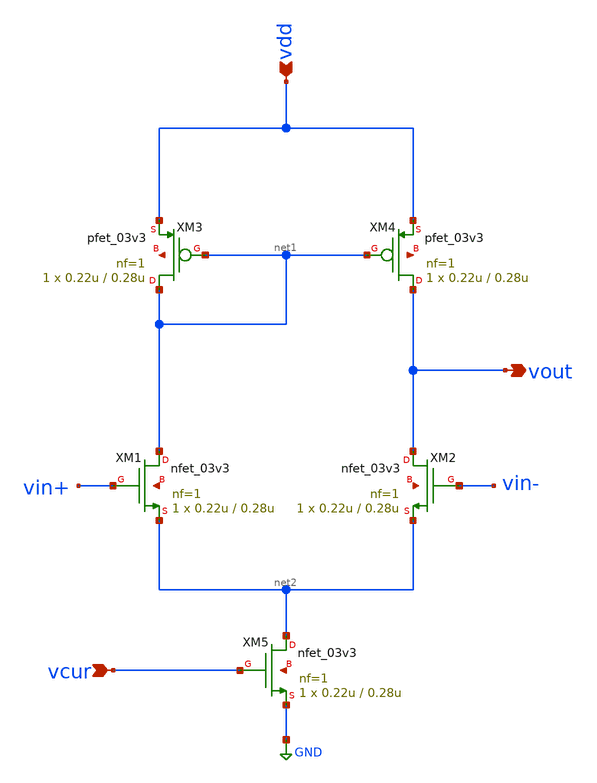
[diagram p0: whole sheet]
** sch_path: designs/5tOTA.sch
**.subckt 5tOTA vdd vout vcur
*.ipin vdd
*.opin vout
*.ipin vcur
XM1 net1 vin+ net2 net3 nfet_03v3 L=0.28u W=0.22u nf=1 ad='int((nf+1)/2) * W/nf * 0.18u' as='int((nf+2)/2) * W/nf * 0.18u'
+ pd='2*int((nf+1)/2) * (W/nf + 0.18u)' ps='2*int((nf+2)/2) * (W/nf + 0.18u)' nrd='0.18u / W' nrs='0.18u / W'
+ sa=0 sb=0 sd=0 m=1
XM2 vout vin- net2 net4 nfet_03v3 L=0.28u W=0.22u nf=1 ad='int((nf+1)/2) * W/nf * 0.18u' as='int((nf+2)/2) * W/nf * 0.18u'
+ pd='2*int((nf+1)/2) * (W/nf + 0.18u)' ps='2*int((nf+2)/2) * (W/nf + 0.18u)' nrd='0.18u / W' nrs='0.18u / W'
+ sa=0 sb=0 sd=0 m=1
XM3 net1 net1 vdd net5 pfet_03v3 L=0.28u W=0.22u nf=1 ad='int((nf+1)/2) * W/nf * 0.18u' as='int((nf+2)/2) * W/nf * 0.18u'
+ pd='2*int((nf+1)/2) * (W/nf + 0.18u)' ps='2*int((nf+2)/2) * (W/nf + 0.18u)' nrd='0.18u / W' nrs='0.18u / W'
+ sa=0 sb=0 sd=0 m=1
XM4 vout net1 vdd net6 pfet_03v3 L=0.28u W=0.22u nf=1 ad='int((nf+1)/2) * W/nf * 0.18u' as='int((nf+2)/2) * W/nf * 0.18u'
+ pd='2*int((nf+1)/2) * (W/nf + 0.18u)' ps='2*int((nf+2)/2) * (W/nf + 0.18u)' nrd='0.18u / W' nrs='0.18u / W'
+ sa=0 sb=0 sd=0 m=1
XM5 net2 vcur GND net7 nfet_03v3 L=0.28u W=0.22u nf=1 ad='int((nf+1)/2) * W/nf * 0.18u' as='int((nf+2)/2) * W/nf * 0.18u'
+ pd='2*int((nf+1)/2) * (W/nf + 0.18u)' ps='2*int((nf+2)/2) * (W/nf + 0.18u)' nrd='0.18u / W' nrs='0.18u / W'
+ sa=0 sb=0 sd=0 m=1
**.ends
.GLOBAL GND
.end
